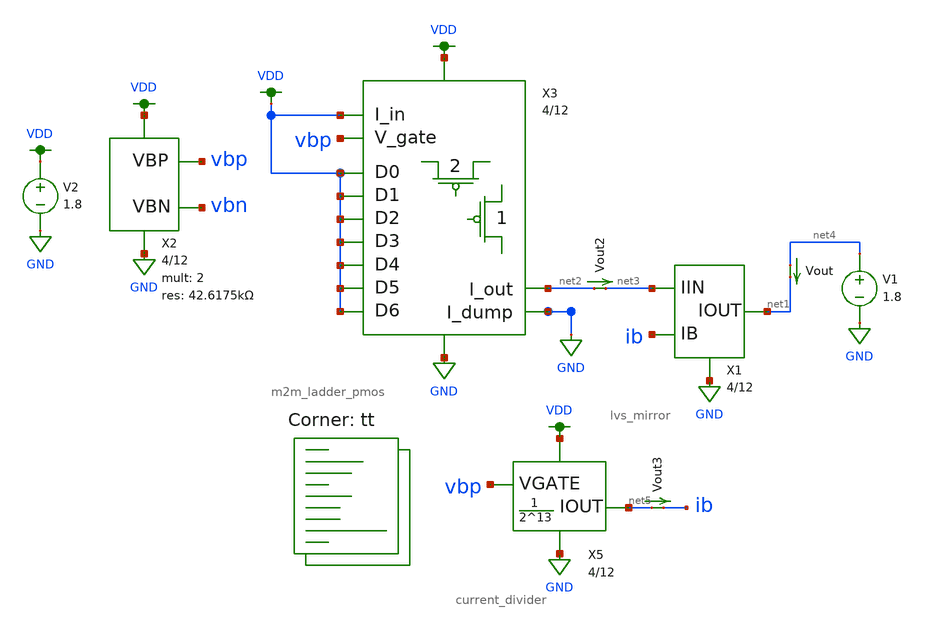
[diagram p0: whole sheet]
** sch_path: dac/schematic/dac_supply_voltage_tb_backup.sch
**.subckt dac_supply_voltage_tb_backup
V2 VDD GND 1.8
X2 vbp VDD GND vbn bias_gen u_w=4 u_l=12 m=2 r=42.6175k
X3 VDD GND VDD VDD VDD VDD VDD VDD VDD vbp VDD GND net2 m2m_ladder_pmos u_w=4 u_l=12
Vout2 net2 net3 0
.save i(vout2)
X1 GND net3 ib net1 lvs_mirror u_w=4 u_l=12 m=2 r=1M
Vout net4 net1 0
.save i(vout)
V1 net4 GND 1.8
X5 GND VDD net5 vbp current_divider u_w=4 u_l=12
Vout3 net5 ib 0
.save i(vout3)
**** begin user architecture code


.control
  set wr_vecnames
  set wr_singlescale
  dc V2 1.75 1.85 0.005
  wrdata ~/documents/git/madvlsi/dac/build/dac_supply_voltage/dac_supply_voltage_tb.txt i(Vout)
.endc

.lib $::SKYWATER_MODELS/sky130.lib.spice tt
**** end user architecture code
**.ends
.GLOBAL GND
.GLOBAL VDD
.end
